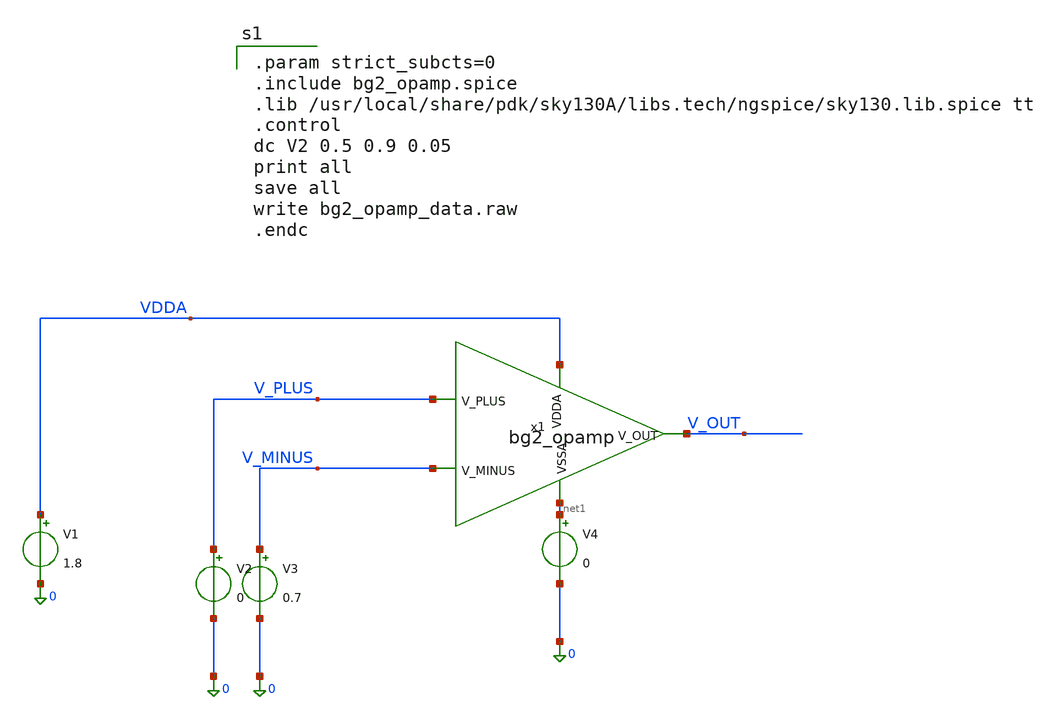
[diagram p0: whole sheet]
** sch_path: lef/lef/gds/bg2_opamp_tb.sch
**.subckt bg2_opamp_tb
V1 VDDA 0 1.8
V2 V_PLUS 0 0
V3 V_MINUS 0 0.7
V4 net1 0 0
x1 VDDA V_OUT V_PLUS V_MINUS net1 bg2_opamp
**** begin user architecture code

.param strict_subcts=0
.include bg2_opamp.spice
.lib /usr/local/share/pdk/sky130A/libs.tech/ngspice/sky130.lib.spice tt
.control
dc V2 0.5 0.9 0.05
print all
save all
write bg2_opamp_data.raw
.endc

**** end user architecture code
**.ends

* expanding   symbol:  bg2_opamp.sym # of pins=5
** sym_path: lef/bg2_opamp.sym
** sch_path: lef/bg2_opamp.sch
.subckt bg2_opamp VDDA V_OUT V_PLUS V_MINUS VSSA
*.ipin VDDA
*.ipin VSSA
*.ipin V_PLUS
*.ipin V_MINUS
*.opin V_OUT
XM3 V_OUT V_PLUS vs VSSA sky130_fd_pr__nfet_01v8 L=6 W=4 nf=1 ad='int((1 + 1)/2) * 4 / 1 * 0.29' as='int((1 + 2)/2) * 4 / 1 * 0.29'
+ pd='2*int((1 + 1)/2) * (4 / 1 + 0.29)' ps='2*int((1 + 2)/2) * (4 / 1 + 0.29)' nrd='0.29 / 4 ' nrs='0.29 / 4 '
+ sa=0 sb=0 sd=0 mult=1 m=1
XM7 V_OUT vb VDDA VDDA sky130_fd_pr__pfet_01v8_lvt L=6 W=4 nf=1 ad='int((1 + 1)/2) * 4 / 1 * 0.29' as='int((1 + 2)/2) * 4 / 1 * 0.29'
+ pd='2*int((1 + 1)/2) * (4 / 1 + 0.29)' ps='2*int((1 + 2)/2) * (4 / 1 + 0.29)' nrd='0.29 / 4 ' nrs='0.29 / 4 '
+ sa=0 sb=0 sd=0 mult=1 m=1
XM8 vb vb VDDA VDDA sky130_fd_pr__pfet_01v8_lvt L=6 W=4 nf=1 ad='int((1 + 1)/2) * 4 / 1 * 0.29' as='int((1 + 2)/2) * 4 / 1 * 0.29'
+ pd='2*int((1 + 1)/2) * (4 / 1 + 0.29)' ps='2*int((1 + 2)/2) * (4 / 1 + 0.29)' nrd='0.29 / 4 ' nrs='0.29 / 4 '
+ sa=0 sb=0 sd=0 mult=1 m=1
XM9 vb V_MINUS vs VSSA sky130_fd_pr__nfet_01v8 L=6 W=4 nf=1 ad='int((1 + 1)/2) * 4 / 1 * 0.29' as='int((1 + 2)/2) * 4 / 1 * 0.29'
+ pd='2*int((1 + 1)/2) * (4 / 1 + 0.29)' ps='2*int((1 + 2)/2) * (4 / 1 + 0.29)' nrd='0.29 / 4 ' nrs='0.29 / 4 '
+ sa=0 sb=0 sd=0 mult=1 m=1
XM10 vs vb VSSA VSSA sky130_fd_pr__nfet_01v8 L=10 W=0.5 nf=1 ad='int((1 + 1)/2) * 0.5 / 1 * 0.29' as='int((1 + 2)/2) * 0.5 / 1 * 0.29'
+ pd='2*int((1 + 1)/2) * (0.5 / 1 + 0.29)' ps='2*int((1 + 2)/2) * (0.5 / 1 + 0.29)' nrd='0.29 / 0.5 ' nrs='0.29 / 0.5 '
+ sa=0 sb=0 sd=0 mult=1 m=1
XM1 V_OUT vb VDDA VDDA sky130_fd_pr__pfet_01v8_lvt L=6 W=4 nf=1 ad='int((1 + 1)/2) * 4 / 1 * 0.29' as='int((1 + 2)/2) * 4 / 1 * 0.29'
+ pd='2*int((1 + 1)/2) * (4 / 1 + 0.29)' ps='2*int((1 + 2)/2) * (4 / 1 + 0.29)' nrd='0.29 / 4 ' nrs='0.29 / 4 '
+ sa=0 sb=0 sd=0 mult=1 m=1
XM2 vb vb VDDA VDDA sky130_fd_pr__pfet_01v8_lvt L=6 W=4 nf=1 ad='int((1 + 1)/2) * 4 / 1 * 0.29' as='int((1 + 2)/2) * 4 / 1 * 0.29'
+ pd='2*int((1 + 1)/2) * (4 / 1 + 0.29)' ps='2*int((1 + 2)/2) * (4 / 1 + 0.29)' nrd='0.29 / 4 ' nrs='0.29 / 4 '
+ sa=0 sb=0 sd=0 mult=1 m=1
XM6 V_OUT V_PLUS vs VSSA sky130_fd_pr__nfet_01v8 L=6 W=4 nf=1 ad='int((1 + 1)/2) * 4 / 1 * 0.29' as='int((1 + 2)/2) * 4 / 1 * 0.29'
+ pd='2*int((1 + 1)/2) * (4 / 1 + 0.29)' ps='2*int((1 + 2)/2) * (4 / 1 + 0.29)' nrd='0.29 / 4 ' nrs='0.29 / 4 '
+ sa=0 sb=0 sd=0 mult=1 m=1
XM4 vb V_MINUS vs VSSA sky130_fd_pr__nfet_01v8 L=6 W=4 nf=1 ad='int((1 + 1)/2) * 4 / 1 * 0.29' as='int((1 + 2)/2) * 4 / 1 * 0.29'
+ pd='2*int((1 + 1)/2) * (4 / 1 + 0.29)' ps='2*int((1 + 2)/2) * (4 / 1 + 0.29)' nrd='0.29 / 4 ' nrs='0.29 / 4 '
+ sa=0 sb=0 sd=0 mult=1 m=1
XM5 vs vb VSSA VSSA sky130_fd_pr__nfet_01v8 L=10 W=0.5 nf=1 ad='int((1 + 1)/2) * 0.5 / 1 * 0.29' as='int((1 + 2)/2) * 0.5 / 1 * 0.29'
+ pd='2*int((1 + 1)/2) * (0.5 / 1 + 0.29)' ps='2*int((1 + 2)/2) * (0.5 / 1 + 0.29)' nrd='0.29 / 0.5 ' nrs='0.29 / 0.5 '
+ sa=0 sb=0 sd=0 mult=1 m=1
.ends

.end
